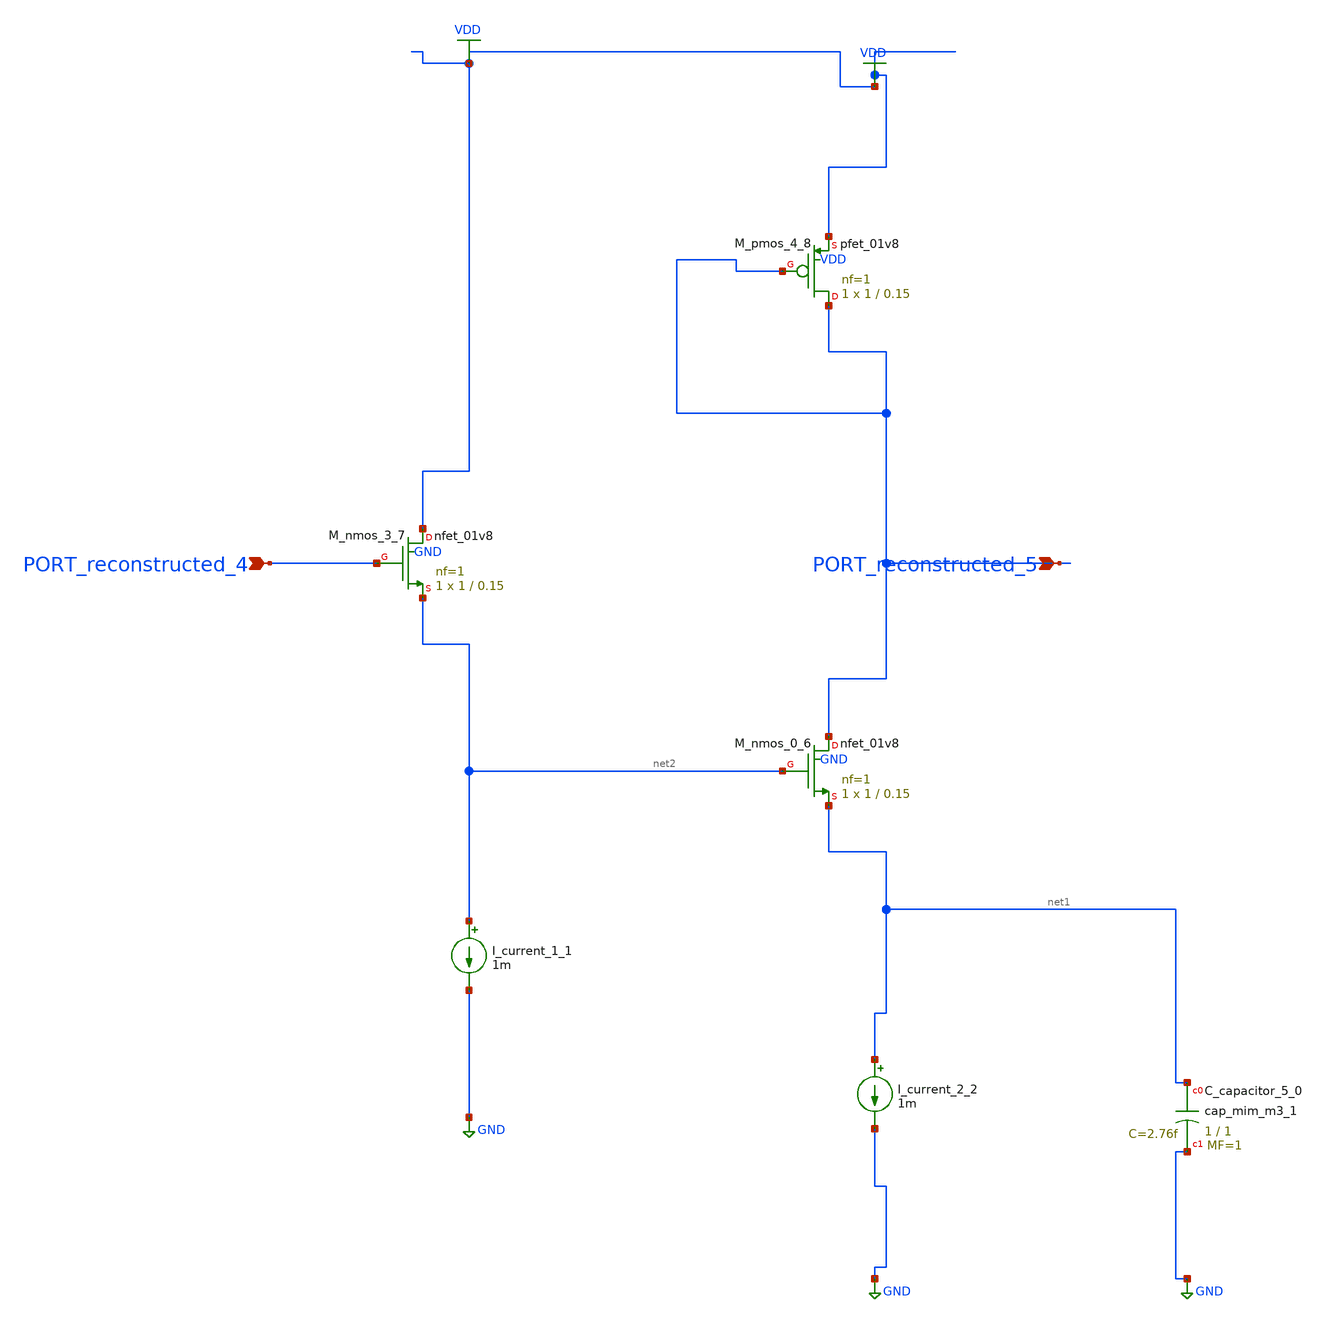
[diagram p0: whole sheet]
** sch_path: schematics/AMSNet/111.sch
**.subckt 111 PORT_reconstructed_5 PORT_reconstructed_4
*.ipin PORT_reconstructed_5
*.ipin PORT_reconstructed_4
XC_capacitor_5_0 net1 GND sky130_fd_pr__cap_mim_m3_1 W=1 L=1 MF=1 m=1
I_current_1_1 net2 GND 1m
I_current_2_2 net1 GND 1m
XM_nmos_0_6 PORT_reconstructed_5 net2 net1 GND sky130_fd_pr__nfet_01v8 L=0.15 W=1 nf=1 ad='int((1 + 1)/2) * 1 / 1 * 0.29'
+ as='int((1 + 2)/2) * 1 / 1 * 0.29' pd='2*int((1 + 1)/2) * (1 / 1 + 0.29)' ps='2*int((1 + 2)/2) * (1 / 1 + 0.29)'
+ nrd='0.29 / 1 ' nrs='0.29 / 1 ' sa=0 sb=0 sd=0 mult=1 m=1
XM_nmos_3_7 VDD PORT_reconstructed_4 net2 GND sky130_fd_pr__nfet_01v8 L=0.15 W=1 nf=1 ad='int((1 + 1)/2) * 1 / 1 * 0.29'
+ as='int((1 + 2)/2) * 1 / 1 * 0.29' pd='2*int((1 + 1)/2) * (1 / 1 + 0.29)' ps='2*int((1 + 2)/2) * (1 / 1 + 0.29)'
+ nrd='0.29 / 1 ' nrs='0.29 / 1 ' sa=0 sb=0 sd=0 mult=1 m=1
XM_pmos_4_8 PORT_reconstructed_5 PORT_reconstructed_5 VDD VDD sky130_fd_pr__pfet_01v8 L=0.15 W=1 nf=1
+ ad='int((1 + 1)/2) * 1 / 1 * 0.29' as='int((1 + 2)/2) * 1 / 1 * 0.29' pd='2*int((1 + 1)/2) * (1 / 1 + 0.29)'
+ ps='2*int((1 + 2)/2) * (1 / 1 + 0.29)' nrd='0.29 / 1 ' nrs='0.29 / 1 ' sa=0 sb=0 sd=0 mult=1 m=1
**.ends
.GLOBAL GND
.GLOBAL VDD
.end
